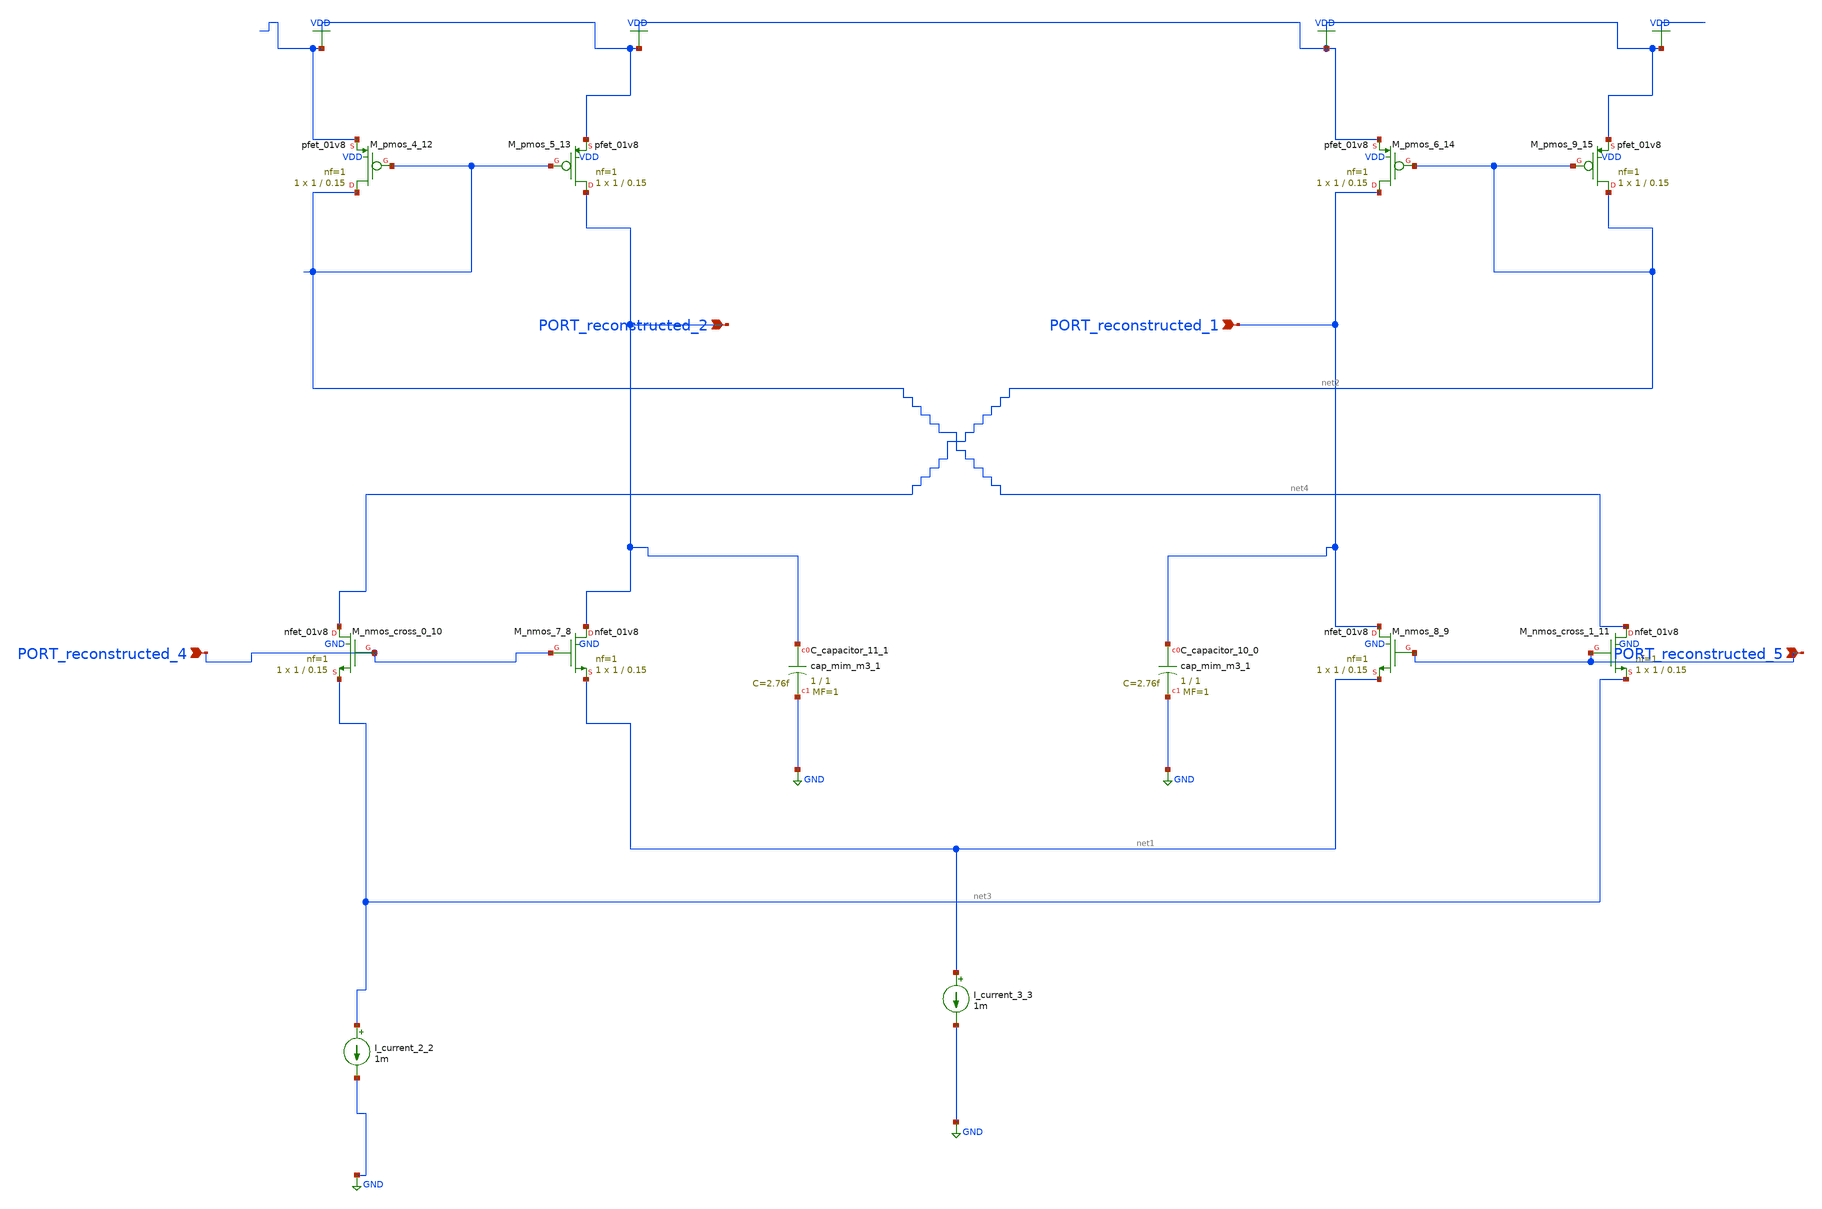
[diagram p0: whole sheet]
** sch_path: schematics/AMSNet/704.sch
**.subckt 704 PORT_reconstructed_4 PORT_reconstructed_5 PORT_reconstructed_1 PORT_reconstructed_2
*.ipin PORT_reconstructed_4
*.ipin PORT_reconstructed_5
*.ipin PORT_reconstructed_1
*.ipin PORT_reconstructed_2
XC_capacitor_10_0 PORT_reconstructed_1 GND sky130_fd_pr__cap_mim_m3_1 W=1 L=1 MF=1 m=1
XC_capacitor_11_1 PORT_reconstructed_2 GND sky130_fd_pr__cap_mim_m3_1 W=1 L=1 MF=1 m=1
I_current_2_2 net3 GND 1m
I_current_3_3 net1 GND 1m
XM_nmos_7_8 PORT_reconstructed_2 PORT_reconstructed_4 net1 GND sky130_fd_pr__nfet_01v8 L=0.15 W=1 nf=1
+ ad='int((1 + 1)/2) * 1 / 1 * 0.29' as='int((1 + 2)/2) * 1 / 1 * 0.29' pd='2*int((1 + 1)/2) * (1 / 1 + 0.29)'
+ ps='2*int((1 + 2)/2) * (1 / 1 + 0.29)' nrd='0.29 / 1 ' nrs='0.29 / 1 ' sa=0 sb=0 sd=0 mult=1 m=1
XM_nmos_8_9 PORT_reconstructed_1 PORT_reconstructed_5 net1 GND sky130_fd_pr__nfet_01v8 L=0.15 W=1 nf=1
+ ad='int((1 + 1)/2) * 1 / 1 * 0.29' as='int((1 + 2)/2) * 1 / 1 * 0.29' pd='2*int((1 + 1)/2) * (1 / 1 + 0.29)'
+ ps='2*int((1 + 2)/2) * (1 / 1 + 0.29)' nrd='0.29 / 1 ' nrs='0.29 / 1 ' sa=0 sb=0 sd=0 mult=1 m=1
XM_nmos_cross_0_10 net2 PORT_reconstructed_4 net3 GND sky130_fd_pr__nfet_01v8 L=0.15 W=1 nf=1 ad='int((1 + 1)/2) * 1 / 1 * 0.29'
+ as='int((1 + 2)/2) * 1 / 1 * 0.29' pd='2*int((1 + 1)/2) * (1 / 1 + 0.29)' ps='2*int((1 + 2)/2) * (1 / 1 + 0.29)'
+ nrd='0.29 / 1 ' nrs='0.29 / 1 ' sa=0 sb=0 sd=0 mult=1 m=1
XM_nmos_cross_1_11 net4 PORT_reconstructed_5 net3 GND sky130_fd_pr__nfet_01v8 L=0.15 W=1 nf=1 ad='int((1 + 1)/2) * 1 / 1 * 0.29'
+ as='int((1 + 2)/2) * 1 / 1 * 0.29' pd='2*int((1 + 1)/2) * (1 / 1 + 0.29)' ps='2*int((1 + 2)/2) * (1 / 1 + 0.29)'
+ nrd='0.29 / 1 ' nrs='0.29 / 1 ' sa=0 sb=0 sd=0 mult=1 m=1
XM_pmos_4_12 net4 net4 VDD VDD sky130_fd_pr__pfet_01v8 L=0.15 W=1 nf=1 ad='int((1 + 1)/2) * 1 / 1 * 0.29'
+ as='int((1 + 2)/2) * 1 / 1 * 0.29' pd='2*int((1 + 1)/2) * (1 / 1 + 0.29)' ps='2*int((1 + 2)/2) * (1 / 1 + 0.29)'
+ nrd='0.29 / 1 ' nrs='0.29 / 1 ' sa=0 sb=0 sd=0 mult=1 m=1
XM_pmos_5_13 PORT_reconstructed_2 net4 VDD VDD sky130_fd_pr__pfet_01v8 L=0.15 W=1 nf=1 ad='int((1 + 1)/2) * 1 / 1 * 0.29'
+ as='int((1 + 2)/2) * 1 / 1 * 0.29' pd='2*int((1 + 1)/2) * (1 / 1 + 0.29)' ps='2*int((1 + 2)/2) * (1 / 1 + 0.29)'
+ nrd='0.29 / 1 ' nrs='0.29 / 1 ' sa=0 sb=0 sd=0 mult=1 m=1
XM_pmos_6_14 PORT_reconstructed_1 net2 VDD VDD sky130_fd_pr__pfet_01v8 L=0.15 W=1 nf=1 ad='int((1 + 1)/2) * 1 / 1 * 0.29'
+ as='int((1 + 2)/2) * 1 / 1 * 0.29' pd='2*int((1 + 1)/2) * (1 / 1 + 0.29)' ps='2*int((1 + 2)/2) * (1 / 1 + 0.29)'
+ nrd='0.29 / 1 ' nrs='0.29 / 1 ' sa=0 sb=0 sd=0 mult=1 m=1
XM_pmos_9_15 net2 net2 VDD VDD sky130_fd_pr__pfet_01v8 L=0.15 W=1 nf=1 ad='int((1 + 1)/2) * 1 / 1 * 0.29'
+ as='int((1 + 2)/2) * 1 / 1 * 0.29' pd='2*int((1 + 1)/2) * (1 / 1 + 0.29)' ps='2*int((1 + 2)/2) * (1 / 1 + 0.29)'
+ nrd='0.29 / 1 ' nrs='0.29 / 1 ' sa=0 sb=0 sd=0 mult=1 m=1
**.ends
.GLOBAL GND
.GLOBAL VDD
.end
